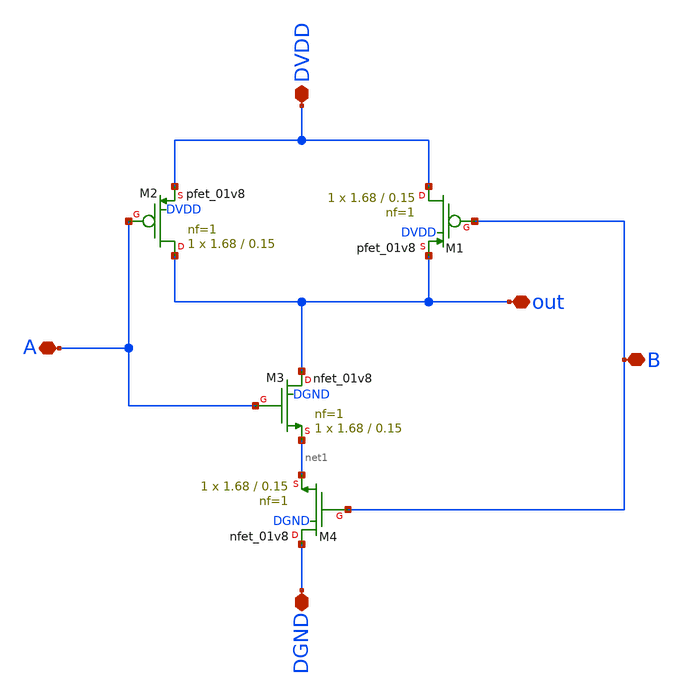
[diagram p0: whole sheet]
** sch_path: tutorial-5/source/nand.sch
**.subckt nand DVDD DGND A B out
*.iopin DVDD
*.iopin DGND
*.iopin A
*.iopin B
*.iopin out
XM1 DVDD B out DVDD sky130_fd_pr__pfet_01v8 L=0.15 W=1.68 nf=1 ad='int((nf+1)/2) * W/nf * 0.29' as='int((nf+2)/2) * W/nf * 0.29'
+ pd='2*int((nf+1)/2) * (W/nf + 0.29)' ps='2*int((nf+2)/2) * (W/nf + 0.29)' nrd='0.29 / W' nrs='0.29 / W'
+ sa=0 sb=0 sd=0 mult=1 m=1
XM2 out A DVDD DVDD sky130_fd_pr__pfet_01v8 L=0.15 W=1.68 nf=1 ad='int((nf+1)/2) * W/nf * 0.29' as='int((nf+2)/2) * W/nf * 0.29'
+ pd='2*int((nf+1)/2) * (W/nf + 0.29)' ps='2*int((nf+2)/2) * (W/nf + 0.29)' nrd='0.29 / W' nrs='0.29 / W'
+ sa=0 sb=0 sd=0 mult=1 m=1
XM3 out A net1 DGND sky130_fd_pr__nfet_01v8 L=0.15 W=1.68 nf=1 ad='int((nf+1)/2) * W/nf * 0.29' as='int((nf+2)/2) * W/nf * 0.29'
+ pd='2*int((nf+1)/2) * (W/nf + 0.29)' ps='2*int((nf+2)/2) * (W/nf + 0.29)' nrd='0.29 / W' nrs='0.29 / W'
+ sa=0 sb=0 sd=0 mult=1 m=1
XM4 DGND B net1 DGND sky130_fd_pr__nfet_01v8 L=0.15 W=1.68 nf=1 ad='int((nf+1)/2) * W/nf * 0.29' as='int((nf+2)/2) * W/nf * 0.29'
+ pd='2*int((nf+1)/2) * (W/nf + 0.29)' ps='2*int((nf+2)/2) * (W/nf + 0.29)' nrd='0.29 / W' nrs='0.29 / W'
+ sa=0 sb=0 sd=0 mult=1 m=1
**.ends
.end
